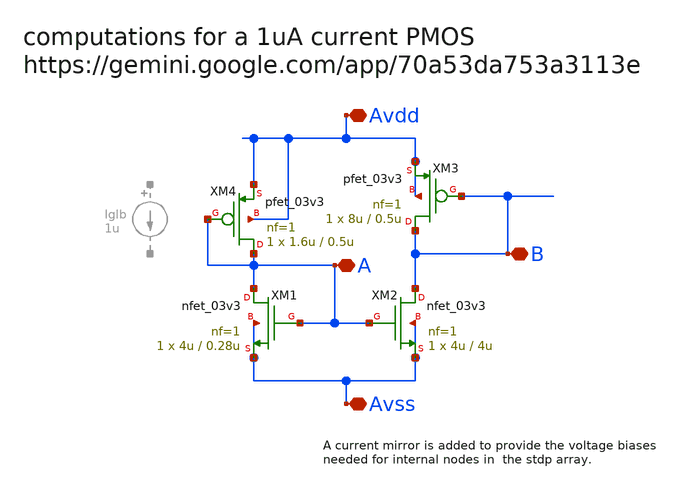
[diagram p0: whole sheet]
** sch_path: designs/libs/snn_analog/current_mirror/sch/current_mirror.sch
**.subckt current_mirror Avdd Avss B A
*.iopin Avdd
*.iopin Avss
*.iopin B
*.iopin A
XM1 A A Avss Avss nfet_03v3 L=0.28u W=4u nf=1 ad='int((nf+1)/2) * W/nf * 0.18u' as='int((nf+2)/2) * W/nf * 0.18u'
+ pd='2*int((nf+1)/2) * (W/nf + 0.18u)' ps='2*int((nf+2)/2) * (W/nf + 0.18u)' nrd='0.18u / W' nrs='0.18u / W'
+ sa=0 sb=0 sd=0 m=1
XM2 B A Avss Avss nfet_03v3 L=4u W=4u nf=1 ad='int((nf+1)/2) * W/nf * 0.18u' as='int((nf+2)/2) * W/nf * 0.18u'
+ pd='2*int((nf+1)/2) * (W/nf + 0.18u)' ps='2*int((nf+2)/2) * (W/nf + 0.18u)' nrd='0.18u / W' nrs='0.18u / W'
+ sa=0 sb=0 sd=0 m=1
XM3 B B Avdd Avdd pfet_03v3 L=0.5u W=8u nf=1 ad='int((nf+1)/2) * W/nf * 0.18u' as='int((nf+2)/2) * W/nf * 0.18u'
+ pd='2*int((nf+1)/2) * (W/nf + 0.18u)' ps='2*int((nf+2)/2) * (W/nf + 0.18u)' nrd='0.18u / W' nrs='0.18u / W'
+ sa=0 sb=0 sd=0 m=1
XM4 A A Avdd Avdd pfet_03v3 L=0.5u W=1.6u nf=1 ad='int((nf+1)/2) * W/nf * 0.18u' as='int((nf+2)/2) * W/nf * 0.18u'
+ pd='2*int((nf+1)/2) * (W/nf + 0.18u)' ps='2*int((nf+2)/2) * (W/nf + 0.18u)' nrd='0.18u / W' nrs='0.18u / W'
+ sa=0 sb=0 sd=0 m=1
**.ends
.end
